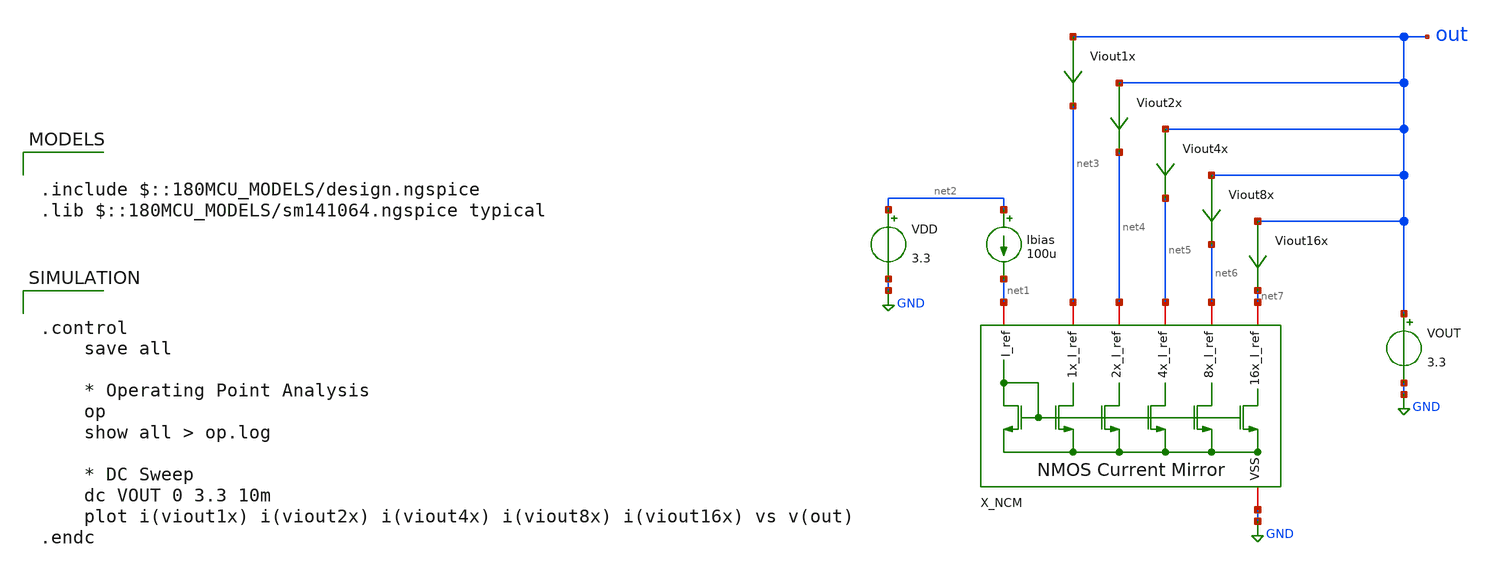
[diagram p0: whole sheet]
** sch_path: designs/libs/tb_current_mirror/tb_nmos_current_mirror.sch
**.subckt tb_nmos_current_mirror
X_NCM net7 net6 net5 net4 net3 net1 GND nmos_current_mirror
VDD net2 GND 3.3
Ibias net2 net1 100u
VOUT out GND 3.3
Viout1x out net3 0
.save i(viout1x)
Viout2x out net4 0
.save i(viout2x)
Viout4x out net5 0
.save i(viout4x)
Viout16x out net7 0
.save i(viout16x)
Viout8x out net6 0
.save i(viout8x)
**** begin user architecture code

.include $::180MCU_MODELS/design.ngspice
.lib $::180MCU_MODELS/sm141064.ngspice typical



.control
    save all

    * Operating Point Analysis
    op
    show all > op.log

    * DC Sweep
    dc VOUT 0 3.3 10m
    plot i(viout1x) i(viout2x) i(viout4x) i(viout8x) i(viout16x) vs v(out)
.endc


**** end user architecture code
**.ends

* expanding   symbol:  libs/core_current_mirror/nmos_current_mirror/nmos_current_mirror.sym # of
*+ pins=7
** sym_path: designs/libs/core_current_mirror/nmos_current_mirror/nmos_current_mirror.sym
** sch_path: designs/libs/core_current_mirror/nmos_current_mirror/nmos_current_mirror.sch
.subckt nmos_current_mirror 16x_I_ref 8x_I_ref 4x_I_ref 2x_I_ref 1x_I_ref I_ref VSS
*.iopin I_ref
*.iopin VSS
*.iopin 1x_I_ref
*.iopin 2x_I_ref
*.iopin 4x_I_ref
*.iopin 8x_I_ref
*.iopin 16x_I_ref
XIREF I_ref VSS I_ref VSS unit_nmos M=1
X1x 1x_I_ref VSS I_ref VSS unit_nmos M=1
X2x 2x_I_ref VSS I_ref VSS unit_nmos M=2
X4x 4x_I_ref VSS I_ref VSS unit_nmos M=4
X8x 8x_I_ref VSS I_ref VSS unit_nmos M=8
X16x 16x_I_ref VSS I_ref VSS unit_nmos M=16
.ends


* expanding   symbol:  libs/core_single_mos/unit_nmos/unit_nmos.sym # of pins=4
** sym_path: libs/core_single_mos/unit_nmos/unit_nmos.sym
** sch_path: libs/core_single_mos/unit_nmos/unit_nmos.sch
.subckt unit_nmos drain sub gate source
*.iopin drain
*.iopin source
*.iopin sub
*.iopin gate
XM1 drain gate source sub nfet_03v3 L=0.5u W=12u nf=2 ad='int((nf+1)/2) * W/nf * 0.18u' as='int((nf+2)/2) * W/nf * 0.18u'
+ pd='2*int((nf+1)/2) * (W/nf + 0.18u)' ps='2*int((nf+2)/2) * (W/nf + 0.18u)' nrd='0.18u / W' nrs='0.18u / W'
+ sa=0 sb=0 sd=0 m={M}
**** begin user architecture code

.param M=1

**** end user architecture code
.ends

.GLOBAL GND
.end
